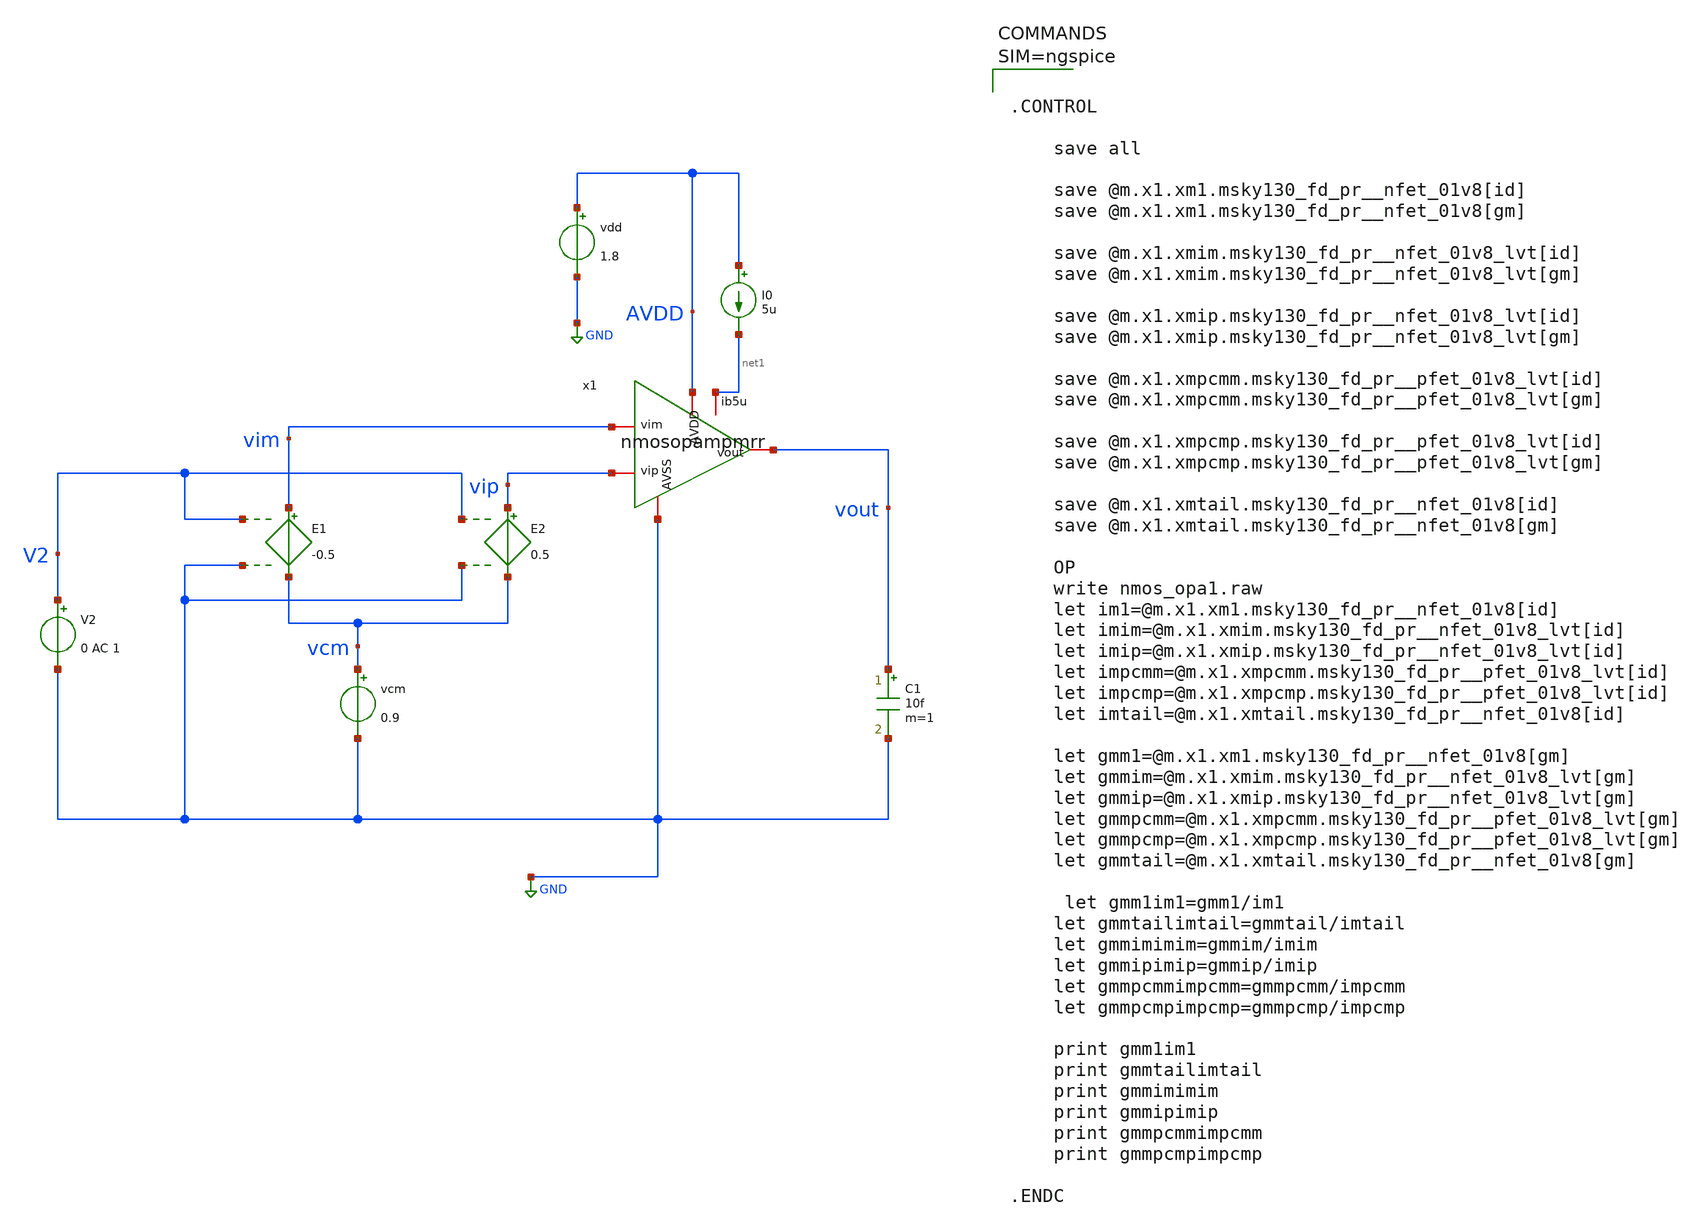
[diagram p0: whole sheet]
** sch_path: work/xschem/nmos_opa1.sch
**.subckt nmos_opa1
E1 vim vcm V2 GND -0.5
E2 vip vcm V2 GND 0.5
V2 V2 GND 0 AC 1
vcm vcm GND 0.9
vdd AVDD GND 1.8
I0 AVDD net1 5u
C1 vout GND 10f m=1
x1 AVDD vout vim vip net1 GND nmosopampmrr
**** begin user architecture code

** opencircuitdesign pdks install
.lib $::SKYWATER_MODELS/sky130.lib.spice tt




.CONTROL

    save all

    save @m.x1.xm1.msky130_fd_pr__nfet_01v8[id]
    save @m.x1.xm1.msky130_fd_pr__nfet_01v8[gm]

    save @m.x1.xmim.msky130_fd_pr__nfet_01v8_lvt[id]
    save @m.x1.xmim.msky130_fd_pr__nfet_01v8_lvt[gm]

    save @m.x1.xmip.msky130_fd_pr__nfet_01v8_lvt[id]
    save @m.x1.xmip.msky130_fd_pr__nfet_01v8_lvt[gm]

    save @m.x1.xmpcmm.msky130_fd_pr__pfet_01v8_lvt[id]
    save @m.x1.xmpcmm.msky130_fd_pr__pfet_01v8_lvt[gm]

    save @m.x1.xmpcmp.msky130_fd_pr__pfet_01v8_lvt[id]
    save @m.x1.xmpcmp.msky130_fd_pr__pfet_01v8_lvt[gm]

    save @m.x1.xmtail.msky130_fd_pr__nfet_01v8[id]
    save @m.x1.xmtail.msky130_fd_pr__nfet_01v8[gm]

    OP
    write nmos_opa1.raw
    let im1=@m.x1.xm1.msky130_fd_pr__nfet_01v8[id]
    let imim=@m.x1.xmim.msky130_fd_pr__nfet_01v8_lvt[id]
    let imip=@m.x1.xmip.msky130_fd_pr__nfet_01v8_lvt[id]
    let impcmm=@m.x1.xmpcmm.msky130_fd_pr__pfet_01v8_lvt[id]
    let impcmp=@m.x1.xmpcmp.msky130_fd_pr__pfet_01v8_lvt[id]
    let imtail=@m.x1.xmtail.msky130_fd_pr__nfet_01v8[id]

    let gmm1=@m.x1.xm1.msky130_fd_pr__nfet_01v8[gm]
    let gmmim=@m.x1.xmim.msky130_fd_pr__nfet_01v8_lvt[gm]
    let gmmip=@m.x1.xmip.msky130_fd_pr__nfet_01v8_lvt[gm]
    let gmmpcmm=@m.x1.xmpcmm.msky130_fd_pr__pfet_01v8_lvt[gm]
    let gmmpcmp=@m.x1.xmpcmp.msky130_fd_pr__pfet_01v8_lvt[gm]
    let gmmtail=@m.x1.xmtail.msky130_fd_pr__nfet_01v8[gm]

 	let gmm1im1=gmm1/im1
	let gmmtailimtail=gmmtail/imtail
	let gmmimimim=gmmim/imim
	let gmmipimip=gmmip/imip
	let gmmpcmmimpcmm=gmmpcmm/impcmm
	let gmmpcmpimpcmp=gmmpcmp/impcmp

	print gmm1im1
	print gmmtailimtail
	print gmmimimim
	print gmmipimip
	print gmmpcmmimpcmm
	print gmmpcmpimpcmp

.ENDC




**** end user architecture code
**.ends

* expanding   symbol:  nmosopampmrr.sym # of pins=6
** sym_path: work/xschem/nmosopampmrr.sym
** sch_path: work/xschem/nmosopampmrr.sch
.subckt nmosopampmrr AVDD vout vim vip ib5u AVSS
*.iopin ib5u
*.iopin vip
*.iopin vim
*.iopin AVDD
*.iopin AVSS
*.iopin vout
**** begin user architecture code



.CONTROL

save all
write nmosopampmrr.raw
set appendfile
write nmosopampmrr.raw

.ENDC



**** end user architecture code
XMtail net1 ib5u AVSS AVSS sky130_fd_pr__nfet_01v8 L=1 W=5 nf=1 ad='int((1 + 1)/2) * 5 / 1 * 0.29' as='int((1 + 2)/2) * 5 / 1 * 0.29'
+ pd='2*int((1 + 1)/2) * (5 / 1 + 0.29)' ps='2*int((1 + 2)/2) * (5 / 1 + 0.29)' nrd='0.29 / 5 ' nrs='0.29 / 5 '
+ sa=0 sb=0 sd=0 mult=2 m=2
XM1 ib5u ib5u AVSS AVSS sky130_fd_pr__nfet_01v8 L=1 W=5 nf=1 ad='int((1 + 1)/2) * 5 / 1 * 0.29' as='int((1 + 2)/2) * 5 / 1 * 0.29'
+ pd='2*int((1 + 1)/2) * (5 / 1 + 0.29)' ps='2*int((1 + 2)/2) * (5 / 1 + 0.29)' nrd='0.29 / 5 ' nrs='0.29 / 5 '
+ sa=0 sb=0 sd=0 mult=1 m=1
XMip vom vip net1 net1 sky130_fd_pr__nfet_01v8_lvt L=2 W=5 nf=1 ad='int((1 + 1)/2) * 5 / 1 * 0.29' as='int((1 + 2)/2) * 5 / 1 * 0.29'
+ pd='2*int((1 + 1)/2) * (5 / 1 + 0.29)' ps='2*int((1 + 2)/2) * (5 / 1 + 0.29)' nrd='0.29 / 5 ' nrs='0.29 / 5 '
+ sa=0 sb=0 sd=0 mult=4 m=4
XMim vout vim net1 net1 sky130_fd_pr__nfet_01v8_lvt L=2 W=5 nf=1 ad='int((1 + 1)/2) * 5 / 1 * 0.29' as='int((1 + 2)/2) * 5 / 1 * 0.29'
+ pd='2*int((1 + 1)/2) * (5 / 1 + 0.29)' ps='2*int((1 + 2)/2) * (5 / 1 + 0.29)' nrd='0.29 / 5 ' nrs='0.29 / 5 '
+ sa=0 sb=0 sd=0 mult=4 m=4
XMpcmm vout vom AVDD AVDD sky130_fd_pr__pfet_01v8_lvt L=2 W=5 nf=1 ad='int((1 + 1)/2) * 5 / 1 * 0.29'
+ as='int((1 + 2)/2) * 5 / 1 * 0.29' pd='2*int((1 + 1)/2) * (5 / 1 + 0.29)' ps='2*int((1 + 2)/2) * (5 / 1 + 0.29)'
+ nrd='0.29 / 5 ' nrs='0.29 / 5 ' sa=0 sb=0 sd=0 mult=2 m=2
XMpcmp vom vom AVDD AVDD sky130_fd_pr__pfet_01v8_lvt L=2 W=5 nf=1 ad='int((1 + 1)/2) * 5 / 1 * 0.29'
+ as='int((1 + 2)/2) * 5 / 1 * 0.29' pd='2*int((1 + 1)/2) * (5 / 1 + 0.29)' ps='2*int((1 + 2)/2) * (5 / 1 + 0.29)'
+ nrd='0.29 / 5 ' nrs='0.29 / 5 ' sa=0 sb=0 sd=0 mult=2 m=2
.ends

.GLOBAL GND
.end
